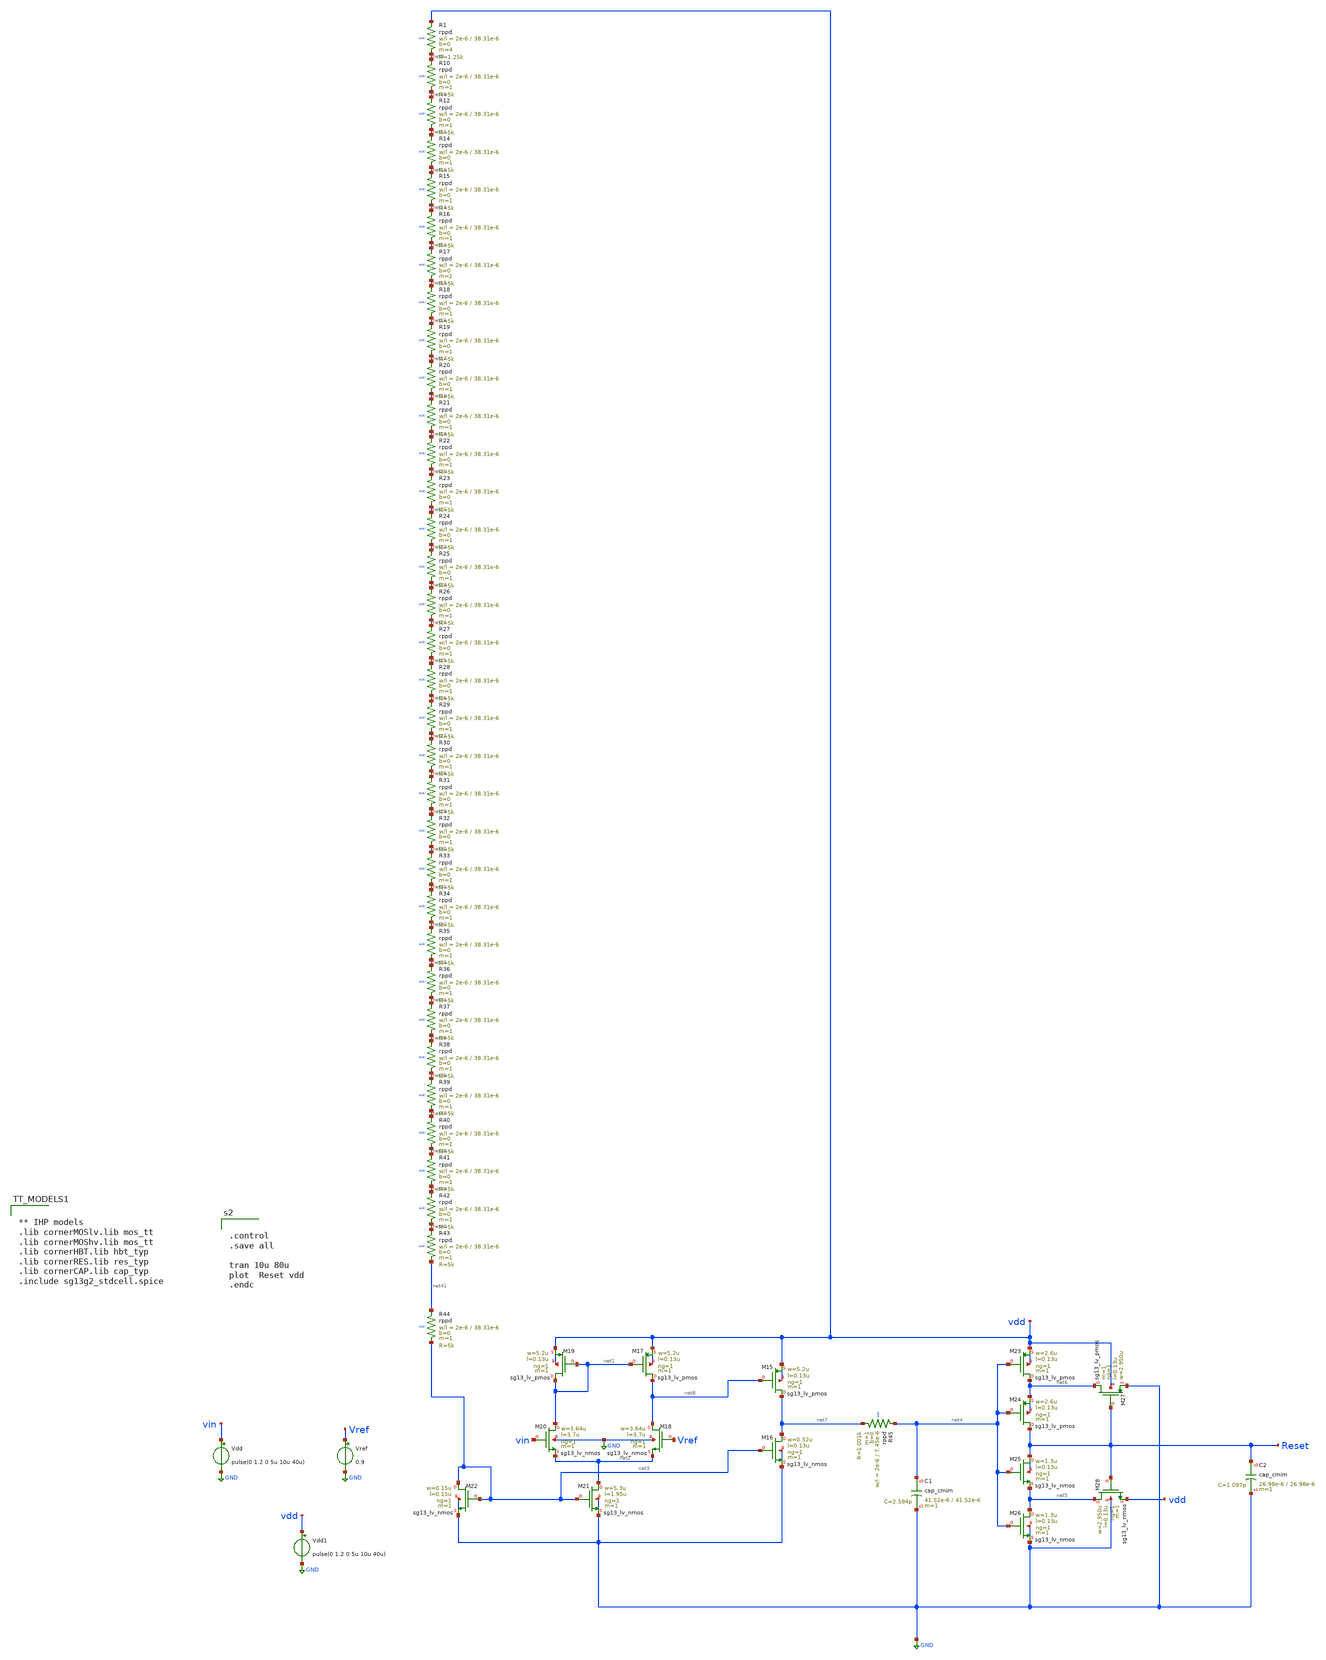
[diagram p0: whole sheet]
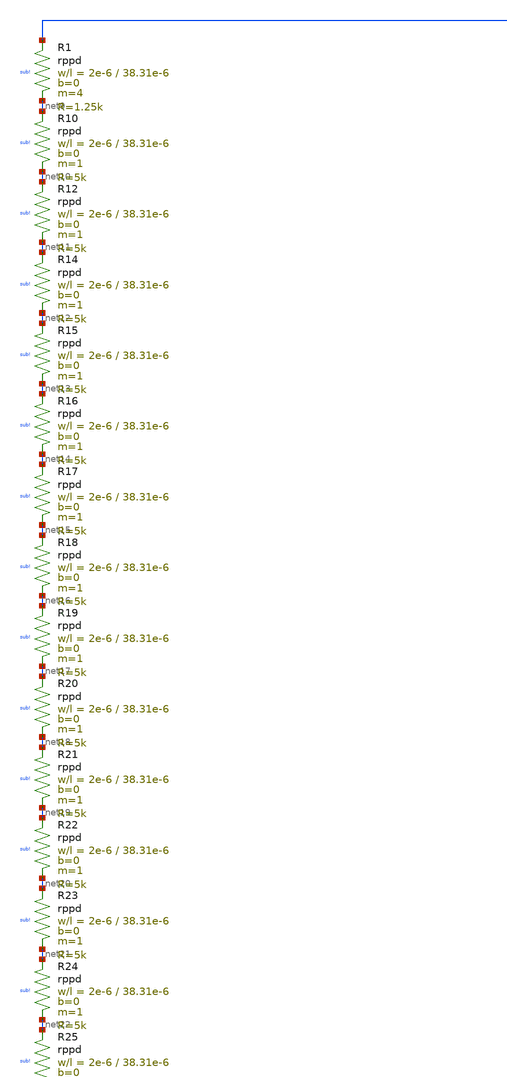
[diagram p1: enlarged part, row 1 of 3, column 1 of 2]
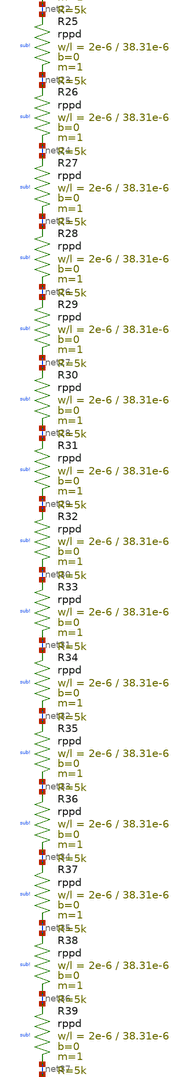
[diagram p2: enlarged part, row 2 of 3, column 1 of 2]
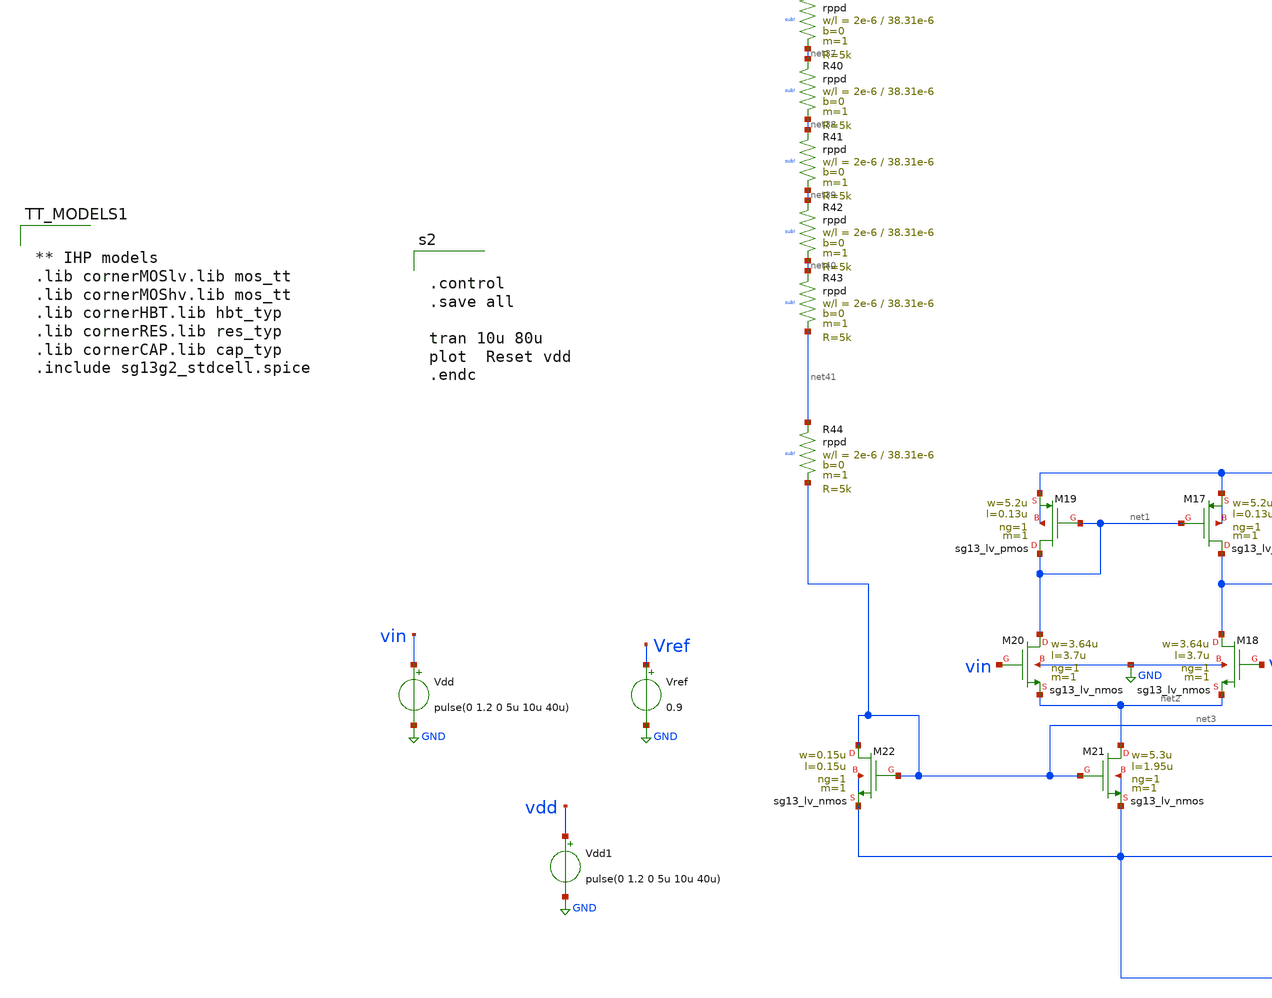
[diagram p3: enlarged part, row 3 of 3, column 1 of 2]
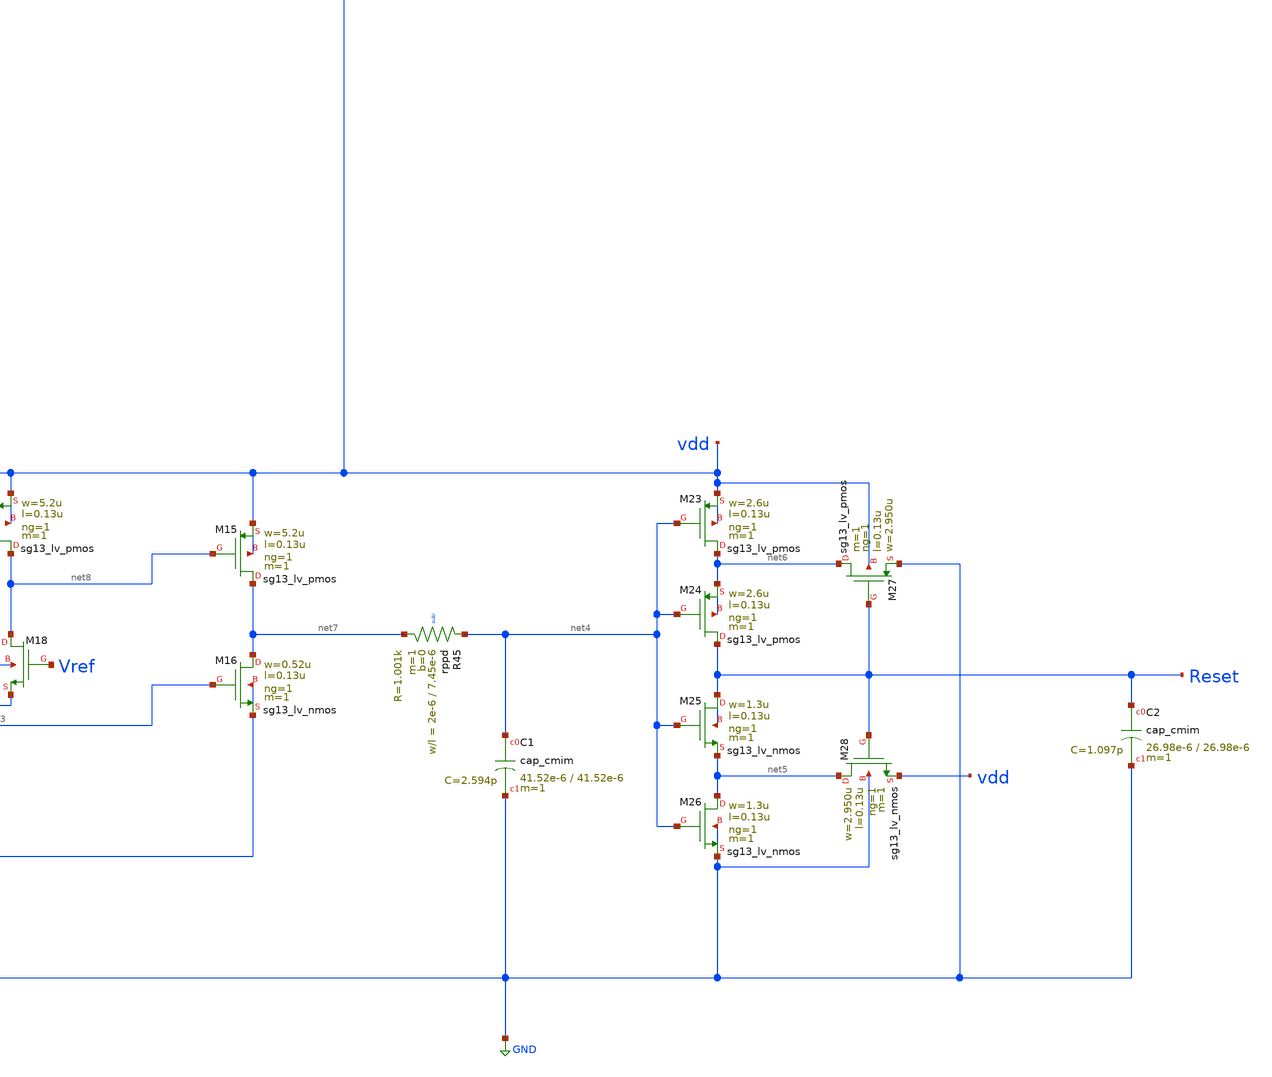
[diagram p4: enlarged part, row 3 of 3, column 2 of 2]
** sch_path: dependencies/POR/POR-main/netlist/schematic/POR_netlist_schematic_layout .sch
**.subckt POR_netlist_schematic_layout
XM15 net7 net8 vdd vdd sg13_lv_pmos w=5.2u l=0.13u ng=1 m=1 mm_ok=1
XM16 net7 net3 GND GND sg13_lv_nmos w=0.52u l=0.13u ng=1 m=1 mm_ok=1
XM17 net8 net1 vdd vdd sg13_lv_pmos w=5.2u l=0.13u ng=1 m=1 mm_ok=1
XM18 net8 Vref net2 GND sg13_lv_nmos w=3.64u l=3.7u ng=1 m=1 mm_ok=1
XM19 net1 net1 vdd vdd sg13_lv_pmos w=5.2u l=0.13u ng=1 m=1 mm_ok=1
XM20 net1 vin net2 GND sg13_lv_nmos w=3.64u l=3.7u ng=1 m=1 mm_ok=1
XM21 net2 net3 GND GND sg13_lv_nmos w=5.3u l=1.95u ng=1 m=1 mm_ok=1
XM22 net3 net3 GND GND sg13_lv_nmos w=0.15u l=0.15u ng=1 m=1 mm_ok=1
XM23 net6 net4 vdd vdd sg13_lv_pmos w=2.6u l=0.13u ng=1 m=1 mm_ok=1
XM24 Reset net4 net6 net6 sg13_lv_pmos w=2.6u l=0.13u ng=1 m=1 mm_ok=1
XM25 Reset net4 net5 Reset sg13_lv_nmos w=1.3u l=0.13u ng=1 m=1 mm_ok=1
XM26 net5 net4 GND GND sg13_lv_nmos w=1.3u l=0.13u ng=1 m=1 mm_ok=1
XM27 net6 Reset GND vdd sg13_lv_pmos w=2.950u l=0.13u ng=1 m=1 mm_ok=1
XM28 net5 Reset vdd GND sg13_lv_nmos w=2.950u l=0.13u ng=1 m=1 mm_ok=1
Vref Vref GND 0.9
Vdd vin GND pulse(0 1.2 0 5u 10u 40u)
XC2 Reset GND cap_cmim w=26.98e-6 l=26.98e-6 m=1 mm_ok=1
XC1 net4 GND cap_cmim w=41.52e-6 l=41.52e-6 m=1 mm_ok=1
XR45 net4 net7 sub! rppd w=2e-6 l=7.45e-6 m=1 b=0 mm_ok=1
Vdd1 vdd GND pulse(0 1.2 0 5u 10u 40u)
XR1 vdd net9 sub! rppd w=2e-6 l=38.31e-6 m=4 b=0 mm_ok=1
XR10 net9 net10 sub! rppd w=2e-6 l=38.31e-6 m=1 b=0 mm_ok=1
XR12 net10 net11 sub! rppd w=2e-6 l=38.31e-6 m=1 b=0 mm_ok=1
XR14 net11 net12 sub! rppd w=2e-6 l=38.31e-6 m=1 b=0 mm_ok=1
XR15 net12 net13 sub! rppd w=2e-6 l=38.31e-6 m=1 b=0 mm_ok=1
XR16 net13 net14 sub! rppd w=2e-6 l=38.31e-6 m=1 b=0 mm_ok=1
XR17 net14 net15 sub! rppd w=2e-6 l=38.31e-6 m=1 b=0 mm_ok=1
XR18 net15 net16 sub! rppd w=2e-6 l=38.31e-6 m=1 b=0 mm_ok=1
XR19 net16 net17 sub! rppd w=2e-6 l=38.31e-6 m=1 b=0 mm_ok=1
XR20 net17 net18 sub! rppd w=2e-6 l=38.31e-6 m=1 b=0 mm_ok=1
XR21 net18 net19 sub! rppd w=2e-6 l=38.31e-6 m=1 b=0 mm_ok=1
XR22 net19 net20 sub! rppd w=2e-6 l=38.31e-6 m=1 b=0 mm_ok=1
XR23 net20 net21 sub! rppd w=2e-6 l=38.31e-6 m=1 b=0 mm_ok=1
XR24 net21 net22 sub! rppd w=2e-6 l=38.31e-6 m=1 b=0 mm_ok=1
XR25 net22 net23 sub! rppd w=2e-6 l=38.31e-6 m=1 b=0 mm_ok=1
XR26 net23 net24 sub! rppd w=2e-6 l=38.31e-6 m=1 b=0 mm_ok=1
XR27 net24 net25 sub! rppd w=2e-6 l=38.31e-6 m=1 b=0 mm_ok=1
XR28 net25 net26 sub! rppd w=2e-6 l=38.31e-6 m=1 b=0 mm_ok=1
XR29 net26 net27 sub! rppd w=2e-6 l=38.31e-6 m=1 b=0 mm_ok=1
XR30 net27 net28 sub! rppd w=2e-6 l=38.31e-6 m=1 b=0 mm_ok=1
XR31 net28 net29 sub! rppd w=2e-6 l=38.31e-6 m=1 b=0 mm_ok=1
XR32 net29 net30 sub! rppd w=2e-6 l=38.31e-6 m=1 b=0 mm_ok=1
XR33 net30 net31 sub! rppd w=2e-6 l=38.31e-6 m=1 b=0 mm_ok=1
XR34 net31 net32 sub! rppd w=2e-6 l=38.31e-6 m=1 b=0 mm_ok=1
XR35 net32 net33 sub! rppd w=2e-6 l=38.31e-6 m=1 b=0 mm_ok=1
XR36 net33 net34 sub! rppd w=2e-6 l=38.31e-6 m=1 b=0 mm_ok=1
XR37 net34 net35 sub! rppd w=2e-6 l=38.31e-6 m=1 b=0 mm_ok=1
XR38 net35 net36 sub! rppd w=2e-6 l=38.31e-6 m=1 b=0 mm_ok=1
XR39 net36 net37 sub! rppd w=2e-6 l=38.31e-6 m=1 b=0 mm_ok=1
XR40 net37 net38 sub! rppd w=2e-6 l=38.31e-6 m=1 b=0 mm_ok=1
XR41 net38 net39 sub! rppd w=2e-6 l=38.31e-6 m=1 b=0 mm_ok=1
XR42 net39 net40 sub! rppd w=2e-6 l=38.31e-6 m=1 b=0 mm_ok=1
XR43 net40 net41 sub! rppd w=2e-6 l=38.31e-6 m=1 b=0 mm_ok=1
XR44 net41 net3 sub! rppd w=2e-6 l=38.31e-6 m=1 b=0 mm_ok=1
**** begin user architecture code


.control
.save all

tran 10u 80u
plot  Reset vdd
.endc




** IHP models
.lib cornerMOSlv.lib mos_tt
.lib cornerMOShv.lib mos_tt
.lib cornerHBT.lib hbt_typ
.lib cornerRES.lib res_typ
.lib cornerCAP.lib cap_typ
.include sg13g2_stdcell.spice


**** end user architecture code
**.ends
.GLOBAL GND
.end
